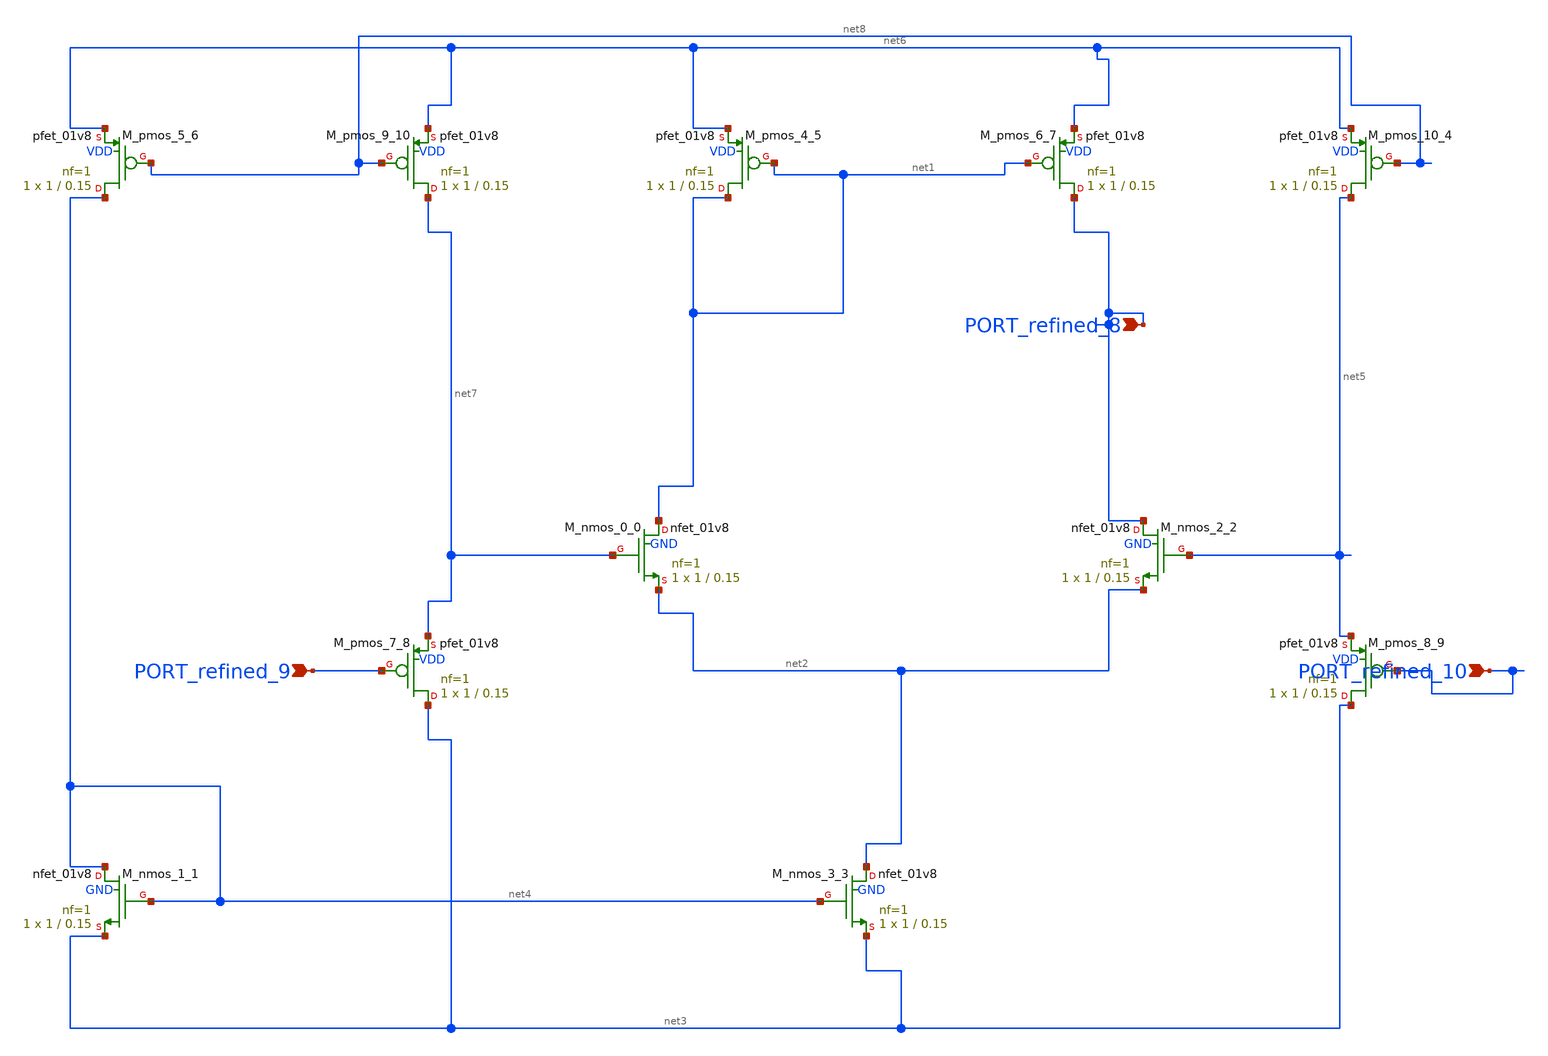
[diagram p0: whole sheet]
** sch_path: schematics/Image2Net/036.sch
**.subckt 036 PORT_refined_8 PORT_refined_10 PORT_refined_9
*.ipin PORT_refined_8
*.ipin PORT_refined_10
*.ipin PORT_refined_9
XM_nmos_0_0 net1 net7 net2 GND sky130_fd_pr__nfet_01v8 L=0.15 W=1 nf=1 ad='int((1 + 1)/2) * 1 / 1 * 0.29'
+ as='int((1 + 2)/2) * 1 / 1 * 0.29' pd='2*int((1 + 1)/2) * (1 / 1 + 0.29)' ps='2*int((1 + 2)/2) * (1 / 1 + 0.29)'
+ nrd='0.29 / 1 ' nrs='0.29 / 1 ' sa=0 sb=0 sd=0 mult=1 m=1
XM_nmos_1_1 net4 net4 net3 GND sky130_fd_pr__nfet_01v8 L=0.15 W=1 nf=1 ad='int((1 + 1)/2) * 1 / 1 * 0.29'
+ as='int((1 + 2)/2) * 1 / 1 * 0.29' pd='2*int((1 + 1)/2) * (1 / 1 + 0.29)' ps='2*int((1 + 2)/2) * (1 / 1 + 0.29)'
+ nrd='0.29 / 1 ' nrs='0.29 / 1 ' sa=0 sb=0 sd=0 mult=1 m=1
XM_nmos_2_2 PORT_refined_8 net5 net2 GND sky130_fd_pr__nfet_01v8 L=0.15 W=1 nf=1 ad='int((1 + 1)/2) * 1 / 1 * 0.29'
+ as='int((1 + 2)/2) * 1 / 1 * 0.29' pd='2*int((1 + 1)/2) * (1 / 1 + 0.29)' ps='2*int((1 + 2)/2) * (1 / 1 + 0.29)'
+ nrd='0.29 / 1 ' nrs='0.29 / 1 ' sa=0 sb=0 sd=0 mult=1 m=1
XM_nmos_3_3 net2 net4 net3 GND sky130_fd_pr__nfet_01v8 L=0.15 W=1 nf=1 ad='int((1 + 1)/2) * 1 / 1 * 0.29'
+ as='int((1 + 2)/2) * 1 / 1 * 0.29' pd='2*int((1 + 1)/2) * (1 / 1 + 0.29)' ps='2*int((1 + 2)/2) * (1 / 1 + 0.29)'
+ nrd='0.29 / 1 ' nrs='0.29 / 1 ' sa=0 sb=0 sd=0 mult=1 m=1
XM_pmos_10_4 net5 net8 net6 VDD sky130_fd_pr__pfet_01v8 L=0.15 W=1 nf=1 ad='int((1 + 1)/2) * 1 / 1 * 0.29'
+ as='int((1 + 2)/2) * 1 / 1 * 0.29' pd='2*int((1 + 1)/2) * (1 / 1 + 0.29)' ps='2*int((1 + 2)/2) * (1 / 1 + 0.29)'
+ nrd='0.29 / 1 ' nrs='0.29 / 1 ' sa=0 sb=0 sd=0 mult=1 m=1
XM_pmos_4_5 net1 net1 net6 VDD sky130_fd_pr__pfet_01v8 L=0.15 W=1 nf=1 ad='int((1 + 1)/2) * 1 / 1 * 0.29'
+ as='int((1 + 2)/2) * 1 / 1 * 0.29' pd='2*int((1 + 1)/2) * (1 / 1 + 0.29)' ps='2*int((1 + 2)/2) * (1 / 1 + 0.29)'
+ nrd='0.29 / 1 ' nrs='0.29 / 1 ' sa=0 sb=0 sd=0 mult=1 m=1
XM_pmos_5_6 net4 net8 net6 VDD sky130_fd_pr__pfet_01v8 L=0.15 W=1 nf=1 ad='int((1 + 1)/2) * 1 / 1 * 0.29'
+ as='int((1 + 2)/2) * 1 / 1 * 0.29' pd='2*int((1 + 1)/2) * (1 / 1 + 0.29)' ps='2*int((1 + 2)/2) * (1 / 1 + 0.29)'
+ nrd='0.29 / 1 ' nrs='0.29 / 1 ' sa=0 sb=0 sd=0 mult=1 m=1
XM_pmos_6_7 PORT_refined_8 net1 net6 VDD sky130_fd_pr__pfet_01v8 L=0.15 W=1 nf=1 ad='int((1 + 1)/2) * 1 / 1 * 0.29'
+ as='int((1 + 2)/2) * 1 / 1 * 0.29' pd='2*int((1 + 1)/2) * (1 / 1 + 0.29)' ps='2*int((1 + 2)/2) * (1 / 1 + 0.29)'
+ nrd='0.29 / 1 ' nrs='0.29 / 1 ' sa=0 sb=0 sd=0 mult=1 m=1
XM_pmos_7_8 net3 PORT_refined_9 net7 VDD sky130_fd_pr__pfet_01v8 L=0.15 W=1 nf=1 ad='int((1 + 1)/2) * 1 / 1 * 0.29'
+ as='int((1 + 2)/2) * 1 / 1 * 0.29' pd='2*int((1 + 1)/2) * (1 / 1 + 0.29)' ps='2*int((1 + 2)/2) * (1 / 1 + 0.29)'
+ nrd='0.29 / 1 ' nrs='0.29 / 1 ' sa=0 sb=0 sd=0 mult=1 m=1
XM_pmos_8_9 net3 PORT_refined_10 net5 VDD sky130_fd_pr__pfet_01v8 L=0.15 W=1 nf=1 ad='int((1 + 1)/2) * 1 / 1 * 0.29'
+ as='int((1 + 2)/2) * 1 / 1 * 0.29' pd='2*int((1 + 1)/2) * (1 / 1 + 0.29)' ps='2*int((1 + 2)/2) * (1 / 1 + 0.29)'
+ nrd='0.29 / 1 ' nrs='0.29 / 1 ' sa=0 sb=0 sd=0 mult=1 m=1
XM_pmos_9_10 net7 net8 net6 VDD sky130_fd_pr__pfet_01v8 L=0.15 W=1 nf=1 ad='int((1 + 1)/2) * 1 / 1 * 0.29'
+ as='int((1 + 2)/2) * 1 / 1 * 0.29' pd='2*int((1 + 1)/2) * (1 / 1 + 0.29)' ps='2*int((1 + 2)/2) * (1 / 1 + 0.29)'
+ nrd='0.29 / 1 ' nrs='0.29 / 1 ' sa=0 sb=0 sd=0 mult=1 m=1
**.ends
.end
